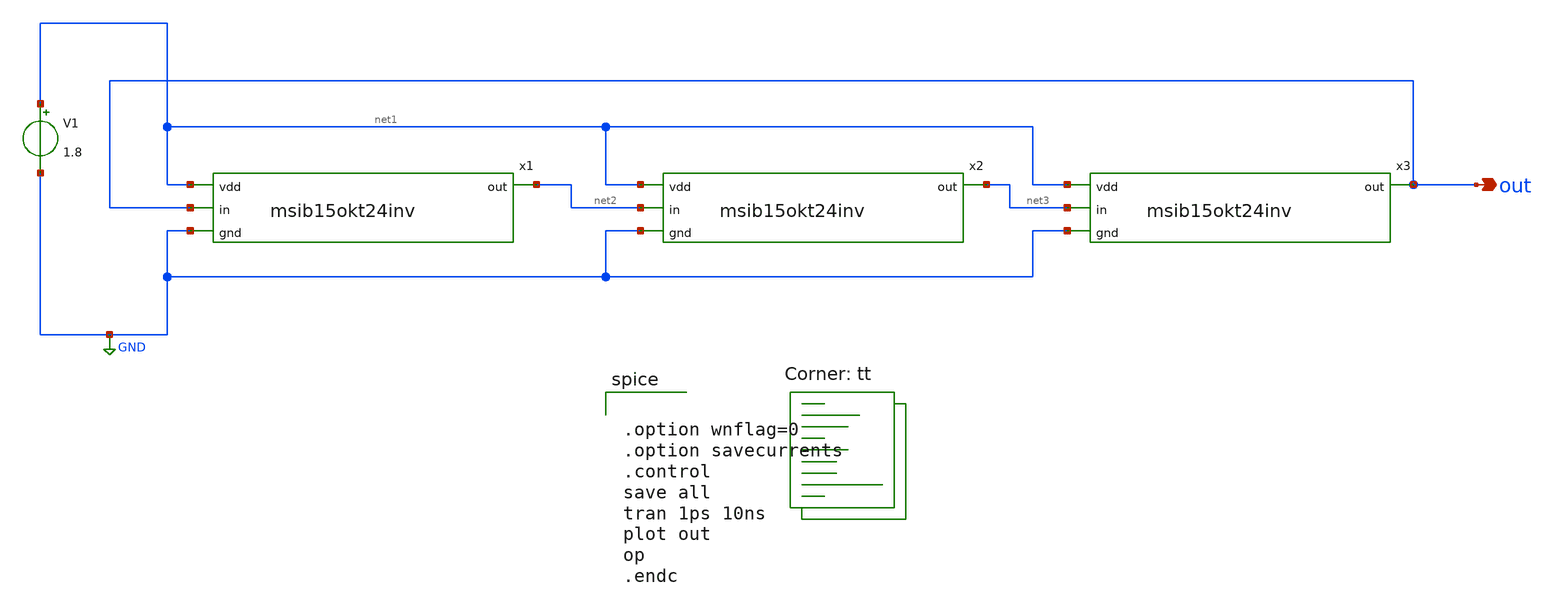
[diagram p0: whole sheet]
** sch_path: Ocilator/SCH/tb_ocilator3.sch
**.subckt tb_ocilator3 out
*.opin out
x1 net1 out net2 GND msib15okt24inv
x2 net1 net2 net3 GND msib15okt24inv
x3 net1 net3 out GND msib15okt24inv
V1 net1 GND 1.8
**** begin user architecture code


.option wnflag=0
.option savecurrents
.control
save all
tran 1ps 10ns
plot out
op
.endc


.lib $::SKYWATER_MODELS/sky130.lib.spice tt
**** end user architecture code
**.ends
.GLOBAL GND
.end
